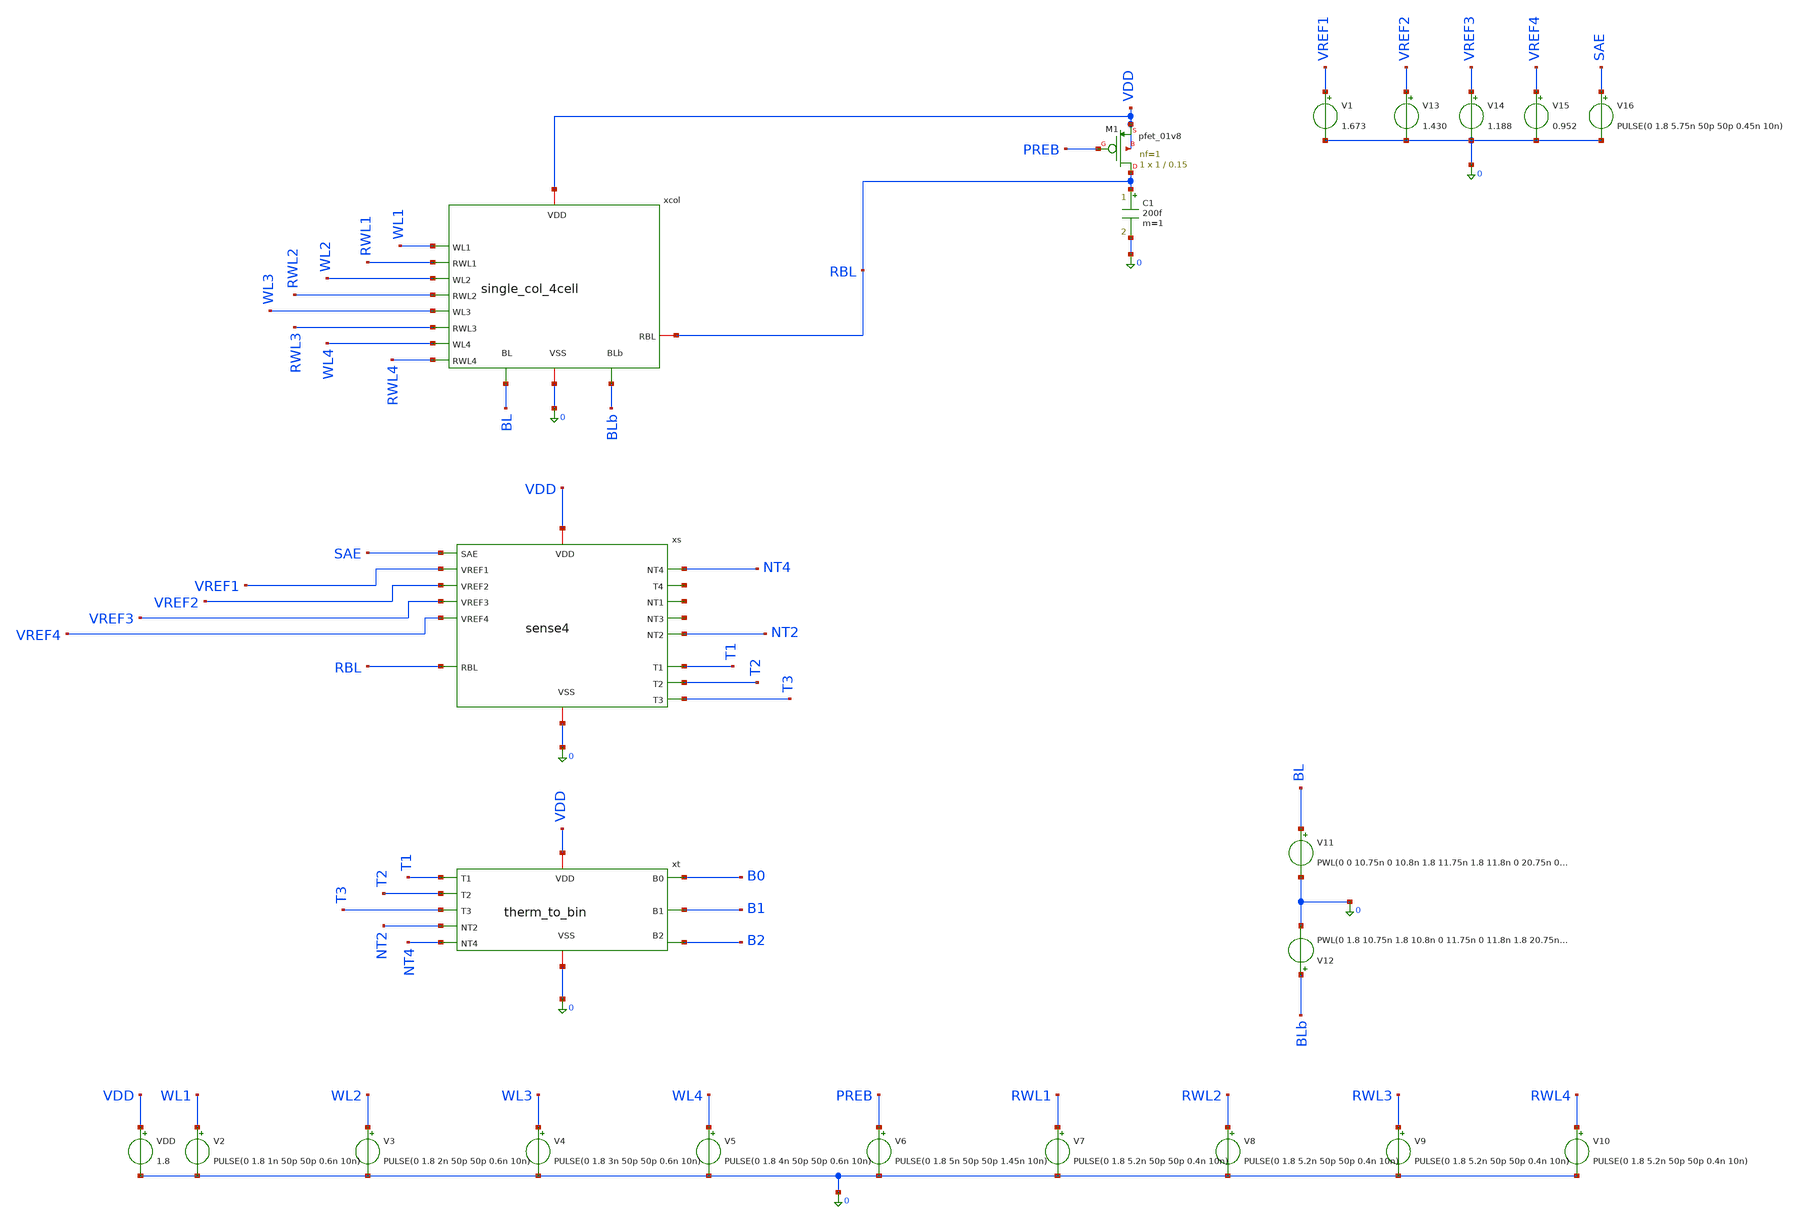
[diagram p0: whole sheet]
** sch_path: schematics/cim_col_4_tb.sch
**.subckt cim_col_4_tb
VDD VDD 0 1.8
V2 WL1 0 PULSE(0 1.8 1n 50p 50p 0.6n 10n)
V3 WL2 0 PULSE(0 1.8 2n 50p 50p 0.6n 10n)
V4 WL3 0 PULSE(0 1.8 3n 50p 50p 0.6n 10n)
V5 WL4 0 PULSE(0 1.8 4n 50p 50p 0.6n 10n)
V6 PREB 0 PULSE(0 1.8 5n 50p 50p 1.45n 10n)
V7 RWL1 0 PULSE(0 1.8 5.2n 50p 50p 0.4n 10n)
V8 RWL2 0 PULSE(0 1.8 5.2n 50p 50p 0.4n 10n)
V9 RWL3 0 PULSE(0 1.8 5.2n 50p 50p 0.4n 10n)
V10 RWL4 0 PULSE(0 1.8 5.2n 50p 50p 0.4n 10n)
V11 BL 0 PWL(0 0 10.75n 0 10.8n 1.8 11.75n 1.8 11.8n 0 20.75n 0 20.8n 1.8 22.75n 1.8 22.8n 0 30.75n
+ 0 30.8n 1.8 33.75n 1.8 33.8n 0 40.75n 0 40.8n 1.8 50.75n 1.8 50.8n 0 51.75n 0 51.8n 1.8 52.75n 1.8
+ 52.8n 0 53.75n 0 53.8n 1.8 60n 1.8)
V12 BLb 0 PWL(0 1.8 10.75n 1.8 10.8n 0 11.75n 0 11.8n 1.8 20.75n 1.8 20.8n 0 22.75n 0 22.8n 1.8
+ 30.75n 1.8 30.8n 0 33.75n 0 33.8n 1.8 40.75n 1.8 40.8n 0 50.75n 0 50.8n 1.8 51.75n 1.8 51.8n 0 52.75n 0
+ 52.8n 1.8 53.75n 1.8 53.8n 0 60n 0)
C1 RBL 0 200f m=1
XM1 RBL PREB VDD VDD sky130_fd_pr__pfet_01v8 L=0.15 W=1 nf=1 ad='int((1 + 1)/2) * 1 / 1 * 0.29' as='int((1 + 2)/2) * 1 / 1 * 0.29'
+ pd='2*int((1 + 1)/2) * (1 / 1 + 0.29)' ps='2*int((1 + 2)/2) * (1 / 1 + 0.29)' nrd='0.29 / 1 ' nrs='0.29 / 1 '
+ sa=0 sb=0 sd=0 mult=1 m=1
xcol WL1 VDD BL BLb RBL RWL1 WL2 RWL2 WL3 RWL3 WL4 RWL4 0 single_col_4cell
xs VDD SAE VREF1 VREF3 VREF2 RBL VREF4 NT4 net1 net2 net3 NT2 0 T1 T2 T3 sense4
xt VDD T3 T1 T2 NT4 NT2 0 B0 B1 B2 therm_to_bin
V1 VREF1 0 1.673
V13 VREF2 0 1.430
V14 VREF3 0 1.188
V15 VREF4 0 0.952
V16 SAE 0 PULSE(0 1.8 5.75n 50p 50p 0.45n 10n)
**** begin user architecture code


.lib /usr/local/share/pdk/sky130A/libs.tech/ngspice/sky130.lib.spice tt
.ic v(xcol.x1.q)=0 v(xcol.x1.qb)=1.8 v(xcol.x2.q)=0 v(xcol.x2.qb)=1.8 v(xcol.x3.q)=0
+ v(xcol.x3.qb)=1.8 v(xcol.x4.q)=0 v(xcol.x4.qb)=1.8 v(rbl)=1.8
.tran 5p 60n uic
.control
run
meas tran p0_b2 FIND v(b2) AT=9.5n
meas tran p0_b1 FIND v(b1) AT=9.5n
meas tran p0_b0 FIND v(b0) AT=9.5n
meas tran p1_b2 FIND v(b2) AT=19.5n
meas tran p1_b1 FIND v(b1) AT=19.5n
meas tran p1_b0 FIND v(b0) AT=19.5n
meas tran p2_b2 FIND v(b2) AT=29.5n
meas tran p2_b1 FIND v(b1) AT=29.5n
meas tran p2_b0 FIND v(b0) AT=29.5n
meas tran p3_b2 FIND v(b2) AT=39.5n
meas tran p3_b1 FIND v(b1) AT=39.5n
meas tran p3_b0 FIND v(b0) AT=39.5n
meas tran p4_b2 FIND v(b2) AT=49.5n
meas tran p4_b1 FIND v(b1) AT=49.5n
meas tran p4_b0 FIND v(b0) AT=49.5n
meas tran p5_b2 FIND v(b2) AT=59.5n
meas tran p5_b1 FIND v(b1) AT=59.5n
meas tran p5_b0 FIND v(b0) AT=59.5n
meas tran q0 INTEG i(vdd) FROM=5n TO=10n
meas tran q4 INTEG i(vdd) FROM=45n TO=50n
let e0 = -1.8*q0
let e4 = -1.8*q4
print e0 e4
meas tran tlat TRIG v(rwl1) VAL=0.9 RISE=1 TD=45n TARG v(b2) VAL=0.9 RISE=1 TD=45n
plot v(sae)+8 v(b2)+6 v(b1)+4 v(b0)+2 v(rbl)
.endc


**** end user architecture code
**.ends
.end
